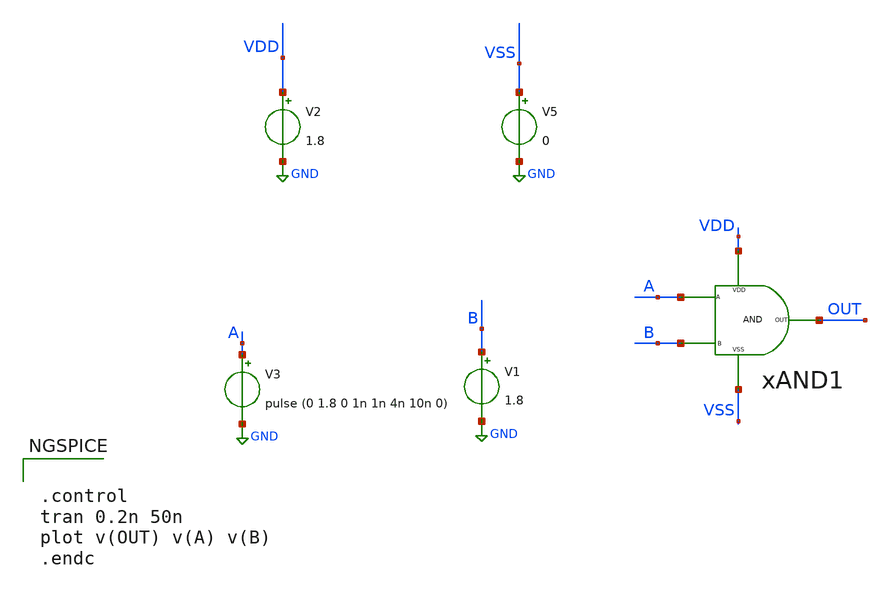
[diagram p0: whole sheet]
** sch_path: xschem/DC_DC_Converter_xschem/DC_DC_Converter/Delay_block_revised/AND_GATE/AND_TB.sch
**.subckt AND_TB
V2 VDD GND 1.8
V5 VSS GND 0
V1 B GND 1.8
V3 A GND pulse (0 1.8 0 1n 1n 4n 10n 0)
xAND1 VDD VSS A B OUT AND
**** begin user architecture code


.control
tran 0.2n 50n
plot v(OUT) v(A) v(B)
.endc


** manual skywater pdks install (with patches applied)
* .lib $::SKYWATER_MODELS/models/sky130.lib.spice tt

** opencircuitdesign pdks install
.lib $::SKYWATER_MODELS/sky130.lib.spice tt
.include $::SKYWATER_STDCELLS/sky130_fd_sc_hd.spice

**** end user architecture code
**.ends

* expanding   symbol:  DC_DC_Converter/Delay_block_revised/AND_GATE/AND.sym # of pins=5
** sym_path: xschem/DC_DC_Converter_xschem/DC_DC_Converter/Delay_block_revised/AND_GATE/AND.sym
** sch_path: xschem/DC_DC_Converter_xschem/DC_DC_Converter/Delay_block_revised/AND_GATE/AND.sch
.subckt AND VDD VSS A B OUT
*.iopin VDD
*.iopin VSS
*.iopin A
*.iopin B
*.iopin OUT
XM2 net2 A net1 VSS sky130_fd_pr__nfet_01v8 L=0.15 W=0.4 nf=1 ad='int((nf+1)/2) * W/nf * 0.29' as='int((nf+2)/2) * W/nf * 0.29'
+ pd='2*int((nf+1)/2) * (W/nf + 0.29)' ps='2*int((nf+2)/2) * (W/nf + 0.29)' nrd='0.29 / W' nrs='0.29 / W'
+ sa=0 sb=0 sd=0 mult=2 m=2
XM3 net2 A VDD VDD sky130_fd_pr__pfet_01v8 L=0.15 W=0.6 nf=1 ad='int((nf+1)/2) * W/nf * 0.29' as='int((nf+2)/2) * W/nf * 0.29'
+ pd='2*int((nf+1)/2) * (W/nf + 0.29)' ps='2*int((nf+2)/2) * (W/nf + 0.29)' nrd='0.29 / W' nrs='0.29 / W'
+ sa=0 sb=0 sd=0 mult=2 m=2
XM4 net1 B VSS VSS sky130_fd_pr__nfet_01v8 L=0.15 W=0.4 nf=1 ad='int((nf+1)/2) * W/nf * 0.29' as='int((nf+2)/2) * W/nf * 0.29'
+ pd='2*int((nf+1)/2) * (W/nf + 0.29)' ps='2*int((nf+2)/2) * (W/nf + 0.29)' nrd='0.29 / W' nrs='0.29 / W'
+ sa=0 sb=0 sd=0 mult=2 m=2
XM5 OUT net2 VSS VSS sky130_fd_pr__nfet_01v8 L=0.15 W=0.4 nf=1 ad='int((nf+1)/2) * W/nf * 0.29' as='int((nf+2)/2) * W/nf * 0.29'
+ pd='2*int((nf+1)/2) * (W/nf + 0.29)' ps='2*int((nf+2)/2) * (W/nf + 0.29)' nrd='0.29 / W' nrs='0.29 / W'
+ sa=0 sb=0 sd=0 mult=1 m=1
XM1 net2 B VDD VDD sky130_fd_pr__pfet_01v8 L=0.15 W=0.6 nf=1 ad='int((nf+1)/2) * W/nf * 0.29' as='int((nf+2)/2) * W/nf * 0.29'
+ pd='2*int((nf+1)/2) * (W/nf + 0.29)' ps='2*int((nf+2)/2) * (W/nf + 0.29)' nrd='0.29 / W' nrs='0.29 / W'
+ sa=0 sb=0 sd=0 mult=2 m=2
XM6 OUT net2 VDD VDD sky130_fd_pr__pfet_01v8 L=0.15 W=0.6 nf=1 ad='int((nf+1)/2) * W/nf * 0.29' as='int((nf+2)/2) * W/nf * 0.29'
+ pd='2*int((nf+1)/2) * (W/nf + 0.29)' ps='2*int((nf+2)/2) * (W/nf + 0.29)' nrd='0.29 / W' nrs='0.29 / W'
+ sa=0 sb=0 sd=0 mult=2 m=2
.ends

.GLOBAL GND
.end
